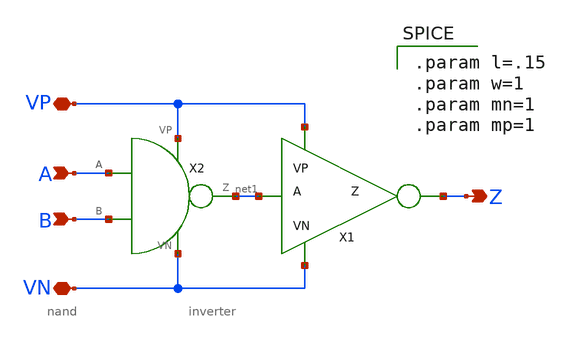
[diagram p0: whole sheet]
** sch_path: schematics/and.sch
**.subckt and A B VP VN Z
*.ipin A
*.ipin B
*.iopin VP
*.iopin VN
*.opin Z
X1 net1 VP VN Z inverter
X2 A B VP VN net1 nand
**** begin user architecture code

.param l=.15
.param w=1
.param mn=1
.param mp=1

**** end user architecture code
**.ends

* expanding   symbol:  /home/madvlsi/Documents/final/xschem/inverter.sym # of pins=4
** sym_path: schematics/inverter.sym
** sch_path: schematics/inverter.sch
.subckt inverter A VP VN Z
*.ipin A
*.iopin VP
*.iopin VN
*.opin Z
XM1 Z A VN GND sky130_fd_pr__nfet_01v8 L=0.15 W=1 nf=1 ad='int((nf+1)/2) * W/nf * 0.29' as='int((nf+2)/2) * W/nf * 0.29'
+ pd='2*int((nf+1)/2) * (W/nf + 0.29)' ps='2*int((nf+2)/2) * (W/nf + 0.29)' nrd='0.29 / W' nrs='0.29 / W'
+ sa=0 sb=0 sd=0 mult=1 m=1
XM2 Z A VP VDD sky130_fd_pr__pfet_01v8 L=0.15 W=1 nf=1 ad='int((nf+1)/2) * W/nf * 0.29' as='int((nf+2)/2) * W/nf * 0.29'
+ pd='2*int((nf+1)/2) * (W/nf + 0.29)' ps='2*int((nf+2)/2) * (W/nf + 0.29)' nrd='0.29 / W' nrs='0.29 / W'
+ sa=0 sb=0 sd=0 mult=2 m=2
**** begin user architecture code

.param l=.15
.param w=1
.param mn=1
.param mp=1

**** end user architecture code
.ends


* expanding   symbol:  /home/madvlsi/Documents/final/xschem/nand.sym # of pins=6
** sym_path: schematics/nand.sym
** sch_path: schematics/nand.sch
.subckt nand A B VP VN Z
*.ipin A
*.iopin VP
*.iopin VN
*.opin Z
*.ipin B
XM1 Z A net1 GND sky130_fd_pr__nfet_01v8 L=0.15 W=1 nf=1 ad='int((nf+1)/2) * W/nf * 0.29' as='int((nf+2)/2) * W/nf * 0.29'
+ pd='2*int((nf+1)/2) * (W/nf + 0.29)' ps='2*int((nf+2)/2) * (W/nf + 0.29)' nrd='0.29 / W' nrs='0.29 / W'
+ sa=0 sb=0 sd=0 mult=1 m=1
XM2 VP B Z VDD sky130_fd_pr__pfet_01v8 L=0.15 W=1 nf=1 ad='int((nf+1)/2) * W/nf * 0.29' as='int((nf+2)/2) * W/nf * 0.29'
+ pd='2*int((nf+1)/2) * (W/nf + 0.29)' ps='2*int((nf+2)/2) * (W/nf + 0.29)' nrd='0.29 / W' nrs='0.29 / W'
+ sa=0 sb=0 sd=0 mult=2 m=2
XM3 VN B net1 GND sky130_fd_pr__nfet_01v8 L=0.15 W=1 nf=1 ad='int((nf+1)/2) * W/nf * 0.29' as='int((nf+2)/2) * W/nf * 0.29'
+ pd='2*int((nf+1)/2) * (W/nf + 0.29)' ps='2*int((nf+2)/2) * (W/nf + 0.29)' nrd='0.29 / W' nrs='0.29 / W'
+ sa=0 sb=0 sd=0 mult=1 m=1
XM4 Z A VP VDD sky130_fd_pr__pfet_01v8 L=0.15 W=1 nf=1 ad='int((nf+1)/2) * W/nf * 0.29' as='int((nf+2)/2) * W/nf * 0.29'
+ pd='2*int((nf+1)/2) * (W/nf + 0.29)' ps='2*int((nf+2)/2) * (W/nf + 0.29)' nrd='0.29 / W' nrs='0.29 / W'
+ sa=0 sb=0 sd=0 mult=2 m=2
.ends

.end
